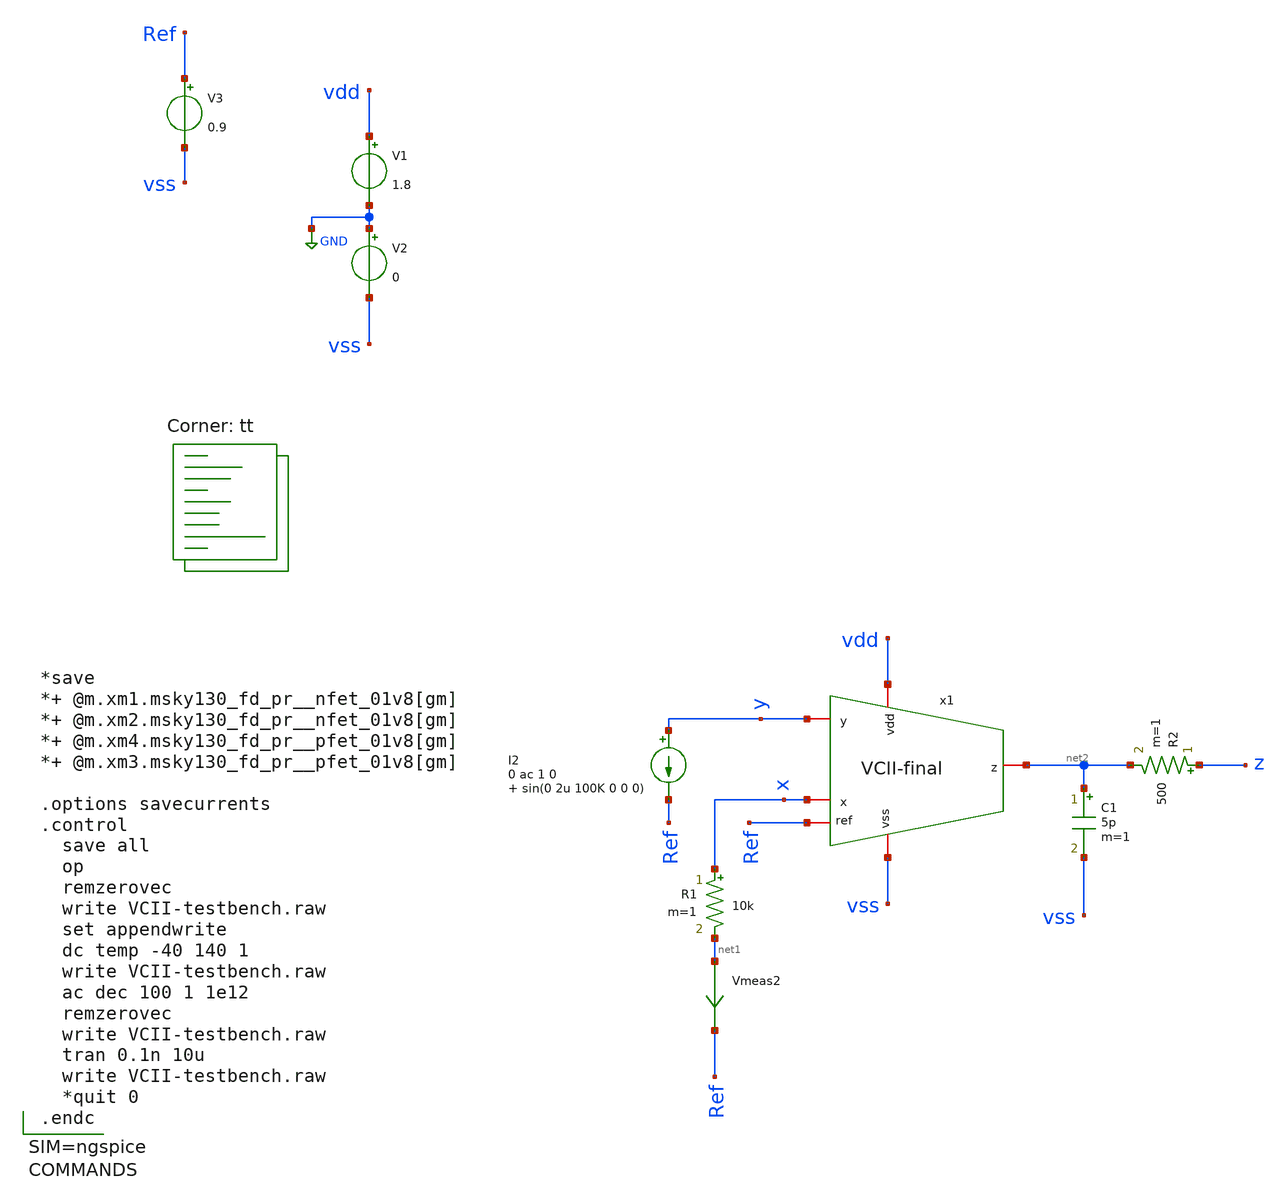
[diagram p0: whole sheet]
** sch_path: xschem/VCII-testbench.sch
**.subckt VCII-testbench
V1 vdd GND 1.8
V2 GND vss 0
V3 Ref vss 0.9
x1 vdd vss net2 y Ref x VCII-final
I2 y Ref 0 ac 1 0 sin(0 2u 100K 0 0 0)
R1 x net1 10k m=1
Vmeas2 net1 Ref 0
.save i(vmeas2)
C1 net2 vss 5p m=1
R2 z net2 500 m=1
**** begin user architecture code



*save
*+ @m.xm1.msky130_fd_pr__nfet_01v8[gm]
*+ @m.xm2.msky130_fd_pr__nfet_01v8[gm]
*+ @m.xm4.msky130_fd_pr__pfet_01v8[gm]
*+ @m.xm3.msky130_fd_pr__pfet_01v8[gm]

.options savecurrents
.control
  save all
  op
  remzerovec
  write VCII-testbench.raw
  set appendwrite
  dc temp -40 140 1
  write VCII-testbench.raw
  ac dec 100 1 1e12
  remzerovec
  write VCII-testbench.raw
  tran 0.1n 10u
  write VCII-testbench.raw
  *quit 0
.endc



.lib $::SKYWATER_MODELS/sky130.lib.spice tt
**** end user architecture code
**.ends

* expanding   symbol:  VCII-final.sym # of pins=6
** sym_path: xschem/VCII-final.sym
** sch_path: xschem/VCII-final.sch
.subckt VCII-final vdd vss z y ref x
*.iopin x
*.iopin y
*.iopin z
*.iopin vdd
*.iopin vss
*.iopin ref
XM1 G1 ref B1 B1 sky130_fd_pr__nfet_01v8 L=0.3 W=10 nf=10 ad='int((nf+1)/2) * W/nf * 0.29' as='int((nf+2)/2) * W/nf * 0.29'
+ pd='2*int((nf+1)/2) * (W/nf + 0.29)' ps='2*int((nf+2)/2) * (W/nf + 0.29)' nrd='0.29 / W' nrs='0.29 / W'
+ sa=0 sb=0 sd=0 mult=5 m=5
XM2 D1 y B1 B1 sky130_fd_pr__nfet_01v8 L=0.3 W=10 nf=10 ad='int((nf+1)/2) * W/nf * 0.29' as='int((nf+2)/2) * W/nf * 0.29'
+ pd='2*int((nf+1)/2) * (W/nf + 0.29)' ps='2*int((nf+2)/2) * (W/nf + 0.29)' nrd='0.29 / W' nrs='0.29 / W'
+ sa=0 sb=0 sd=0 mult=5 m=5
XM3 D1 G1 vdd vdd sky130_fd_pr__pfet_01v8 L=1 W=5 nf=5 ad='int((nf+1)/2) * W/nf * 0.29' as='int((nf+2)/2) * W/nf * 0.29'
+ pd='2*int((nf+1)/2) * (W/nf + 0.29)' ps='2*int((nf+2)/2) * (W/nf + 0.29)' nrd='0.29 / W' nrs='0.29 / W'
+ sa=0 sb=0 sd=0 mult=1 m=1
XM4 G1 G1 vdd vdd sky130_fd_pr__pfet_01v8 L=1 W=5 nf=5 ad='int((nf+1)/2) * W/nf * 0.29' as='int((nf+2)/2) * W/nf * 0.29'
+ pd='2*int((nf+1)/2) * (W/nf + 0.29)' ps='2*int((nf+2)/2) * (W/nf + 0.29)' nrd='0.29 / W' nrs='0.29 / W'
+ sa=0 sb=0 sd=0 mult=1 m=1
XM5 B1 G2 vss vss sky130_fd_pr__nfet_01v8 L=2 W=10 nf=10 ad='int((nf+1)/2) * W/nf * 0.29' as='int((nf+2)/2) * W/nf * 0.29'
+ pd='2*int((nf+1)/2) * (W/nf + 0.29)' ps='2*int((nf+2)/2) * (W/nf + 0.29)' nrd='0.29 / W' nrs='0.29 / W'
+ sa=0 sb=0 sd=0 mult=1 m=1
XM6 G2 G2 vss vss sky130_fd_pr__nfet_01v8 L=2 W=10 nf=10 ad='int((nf+1)/2) * W/nf * 0.29' as='int((nf+2)/2) * W/nf * 0.29'
+ pd='2*int((nf+1)/2) * (W/nf + 0.29)' ps='2*int((nf+2)/2) * (W/nf + 0.29)' nrd='0.29 / W' nrs='0.29 / W'
+ sa=0 sb=0 sd=0 mult=1 m=1
XM7 G3 D1 y y sky130_fd_pr__nfet_01v8 L=0.3 W=40 nf=20 ad='int((nf+1)/2) * W/nf * 0.29' as='int((nf+2)/2) * W/nf * 0.29'
+ pd='2*int((nf+1)/2) * (W/nf + 0.29)' ps='2*int((nf+2)/2) * (W/nf + 0.29)' nrd='0.29 / W' nrs='0.29 / W'
+ sa=0 sb=0 sd=0 mult=1 m=1
XM8 y G2 vss vss sky130_fd_pr__nfet_01v8 L=2 W=10 nf=10 ad='int((nf+1)/2) * W/nf * 0.29' as='int((nf+2)/2) * W/nf * 0.29'
+ pd='2*int((nf+1)/2) * (W/nf + 0.29)' ps='2*int((nf+2)/2) * (W/nf + 0.29)' nrd='0.29 / W' nrs='0.29 / W'
+ sa=0 sb=0 sd=0 mult=1 m=1
XM9 G3 G3 vdd vdd sky130_fd_pr__pfet_01v8 L=1 W=50 nf=20 ad='int((nf+1)/2) * W/nf * 0.29' as='int((nf+2)/2) * W/nf * 0.29'
+ pd='2*int((nf+1)/2) * (W/nf + 0.29)' ps='2*int((nf+2)/2) * (W/nf + 0.29)' nrd='0.29 / W' nrs='0.29 / W'
+ sa=0 sb=0 sd=0 mult=10 m=10
XM10 x G3 vdd vdd sky130_fd_pr__pfet_01v8 L=1 W=50 nf=20 ad='int((nf+1)/2) * W/nf * 0.29' as='int((nf+2)/2) * W/nf * 0.29'
+ pd='2*int((nf+1)/2) * (W/nf + 0.29)' ps='2*int((nf+2)/2) * (W/nf + 0.29)' nrd='0.29 / W' nrs='0.29 / W'
+ sa=0 sb=0 sd=0 mult=10 m=10
XM11 x G2 vss vss sky130_fd_pr__nfet_01v8 L=2 W=10 nf=10 ad='int((nf+1)/2) * W/nf * 0.29' as='int((nf+2)/2) * W/nf * 0.29'
+ pd='2*int((nf+1)/2) * (W/nf + 0.29)' ps='2*int((nf+2)/2) * (W/nf + 0.29)' nrd='0.29 / W' nrs='0.29 / W'
+ sa=0 sb=0 sd=0 mult=1 m=1
XM14 net1 G2 vss vss sky130_fd_pr__nfet_01v8 L=2 W=10 nf=10 ad='int((nf+1)/2) * W/nf * 0.29' as='int((nf+2)/2) * W/nf * 0.29'
+ pd='2*int((nf+1)/2) * (W/nf + 0.29)' ps='2*int((nf+2)/2) * (W/nf + 0.29)' nrd='0.29 / W' nrs='0.29 / W'
+ sa=0 sb=0 sd=0 mult=1 m=1
XM12 z G2 vss vss sky130_fd_pr__nfet_01v8 L=2.3 W=5 nf=5 ad='int((nf+1)/2) * W/nf * 0.29' as='int((nf+2)/2) * W/nf * 0.29'
+ pd='2*int((nf+1)/2) * (W/nf + 0.29)' ps='2*int((nf+2)/2) * (W/nf + 0.29)' nrd='0.29 / W' nrs='0.29 / W'
+ sa=0 sb=0 sd=0 mult=1 m=1
XM15 vdd G4 z z sky130_fd_pr__nfet_01v8 L=0.15 W=50 nf=10 ad='int((nf+1)/2) * W/nf * 0.29' as='int((nf+2)/2) * W/nf * 0.29'
+ pd='2*int((nf+1)/2) * (W/nf + 0.29)' ps='2*int((nf+2)/2) * (W/nf + 0.29)' nrd='0.29 / W' nrs='0.29 / W'
+ sa=0 sb=0 sd=0 mult=2 m=2
XM13 net1 net1 vdd vdd sky130_fd_pr__pfet_01v8 L=1 W=5 nf=1 ad='int((nf+1)/2) * W/nf * 0.29' as='int((nf+2)/2) * W/nf * 0.29'
+ pd='2*int((nf+1)/2) * (W/nf + 0.29)' ps='2*int((nf+2)/2) * (W/nf + 0.29)' nrd='0.29 / W' nrs='0.29 / W'
+ sa=0 sb=0 sd=0 mult=1 m=1
XM16 G4 net1 vdd vdd sky130_fd_pr__pfet_01v8 L=1 W=5 nf=1 ad='int((nf+1)/2) * W/nf * 0.29' as='int((nf+2)/2) * W/nf * 0.29'
+ pd='2*int((nf+1)/2) * (W/nf + 0.29)' ps='2*int((nf+2)/2) * (W/nf + 0.29)' nrd='0.29 / W' nrs='0.29 / W'
+ sa=0 sb=0 sd=0 mult=1 m=1
XM17 vss x G4 G4 sky130_fd_pr__pfet_01v8 L=0.15 W=50 nf=10 ad='int((nf+1)/2) * W/nf * 0.29' as='int((nf+2)/2) * W/nf * 0.29'
+ pd='2*int((nf+1)/2) * (W/nf + 0.29)' ps='2*int((nf+2)/2) * (W/nf + 0.29)' nrd='0.29 / W' nrs='0.29 / W'
+ sa=0 sb=0 sd=0 mult=1 m=1
XR13 net2 vdd vss sky130_fd_pr__res_xhigh_po W=0.35 L=8 mult=1 m=1
XR1 net3 net2 vss sky130_fd_pr__res_xhigh_po W=0.35 L=8 mult=1 m=1
XR3 net4 net3 vss sky130_fd_pr__res_xhigh_po W=0.35 L=8 mult=1 m=1
XR6 net5 G2 vss sky130_fd_pr__res_high_po W=0.35 L=10.5 mult=1 m=1
XR7 net6 net5 vss sky130_fd_pr__res_high_po W=0.35 L=10.5 mult=1 m=1
XR4 net4 net6 vss sky130_fd_pr__res_high_po W=0.35 L=10.5 mult=1 m=1
.ends

.GLOBAL GND
.end
